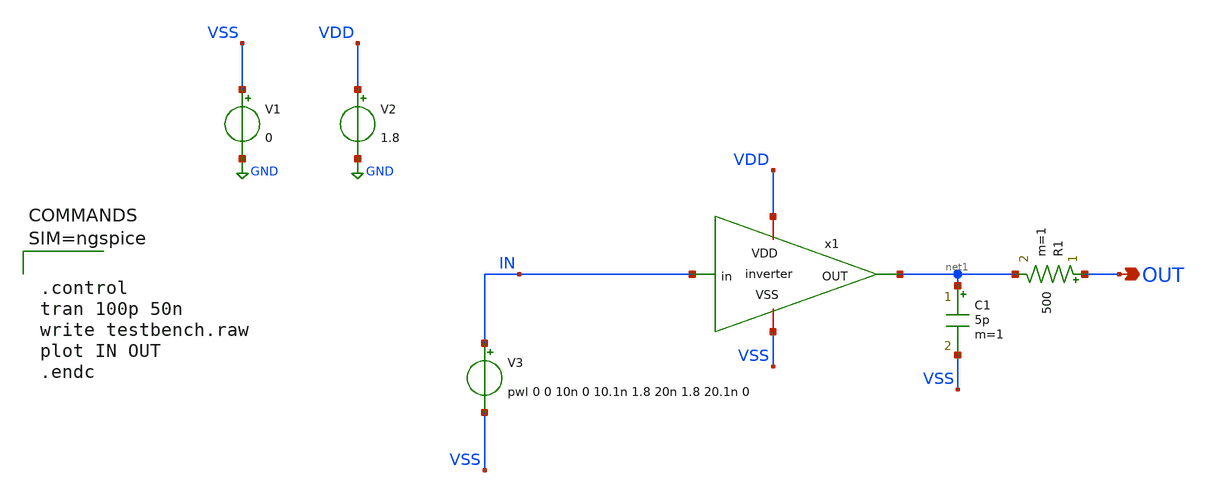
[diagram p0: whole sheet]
** sch_path: xschem/testbench.sch
**.subckt testbench OUT
*.opin OUT
x1 VDD VSS net1 IN inverter
V1 VSS GND 0
V2 VDD GND 1.8
C1 net1 VSS 5p m=1
R1 OUT net1 500 m=1
V3 IN VSS pwl 0 0 10n 0 10.1n 1.8 20n 1.8 20.1n 0
**** begin user architecture code

** opencircuitdesign pdks install
.lib $::SKYWATER_MODELS/sky130.lib.spice tt





.control
tran 100p 50n
write testbench.raw
plot IN OUT
.endc



**** end user architecture code
**.ends

* expanding   symbol:  inverter.sym # of pins=4
** sym_path: xschem/inverter.sym
** sch_path: xschem/inverter.sch
.subckt inverter VDD VSS OUT in
*.iopin VDD
*.iopin VSS
*.ipin in
*.opin OUT
XM1 outm in VSS VSS sky130_fd_pr__nfet_01v8_lvt L=0.15 W=1 nf=1 ad='int((nf+1)/2) * W/nf * 0.29' as='int((nf+2)/2) * W/nf * 0.29'
+ pd='2*int((nf+1)/2) * (W/nf + 0.29)' ps='2*int((nf+2)/2) * (W/nf + 0.29)' nrd='0.29 / W' nrs='0.29 / W'
+ sa=0 sb=0 sd=0 mult=1 m=1
XM2 outm in VDD VDD sky130_fd_pr__pfet_01v8_lvt L=0.35 W=2 nf=1 ad='int((nf+1)/2) * W/nf * 0.29' as='int((nf+2)/2) * W/nf * 0.29'
+ pd='2*int((nf+1)/2) * (W/nf + 0.29)' ps='2*int((nf+2)/2) * (W/nf + 0.29)' nrd='0.29 / W' nrs='0.29 / W'
+ sa=0 sb=0 sd=0 mult=1 m=1
XM3 OUT outm VSS VSS sky130_fd_pr__nfet_01v8_lvt L=0.15 W=8 nf=1 ad='int((nf+1)/2) * W/nf * 0.29' as='int((nf+2)/2) * W/nf * 0.29'
+ pd='2*int((nf+1)/2) * (W/nf + 0.29)' ps='2*int((nf+2)/2) * (W/nf + 0.29)' nrd='0.29 / W' nrs='0.29 / W'
+ sa=0 sb=0 sd=0 mult=1 m=1
XM4 OUT outm VDD VDD sky130_fd_pr__pfet_01v8_lvt L=0.35 W=16 nf=1 ad='int((nf+1)/2) * W/nf * 0.29' as='int((nf+2)/2) * W/nf * 0.29'
+ pd='2*int((nf+1)/2) * (W/nf + 0.29)' ps='2*int((nf+2)/2) * (W/nf + 0.29)' nrd='0.29 / W' nrs='0.29 / W'
+ sa=0 sb=0 sd=0 mult=1 m=1
.ends

.GLOBAL GND
.end
